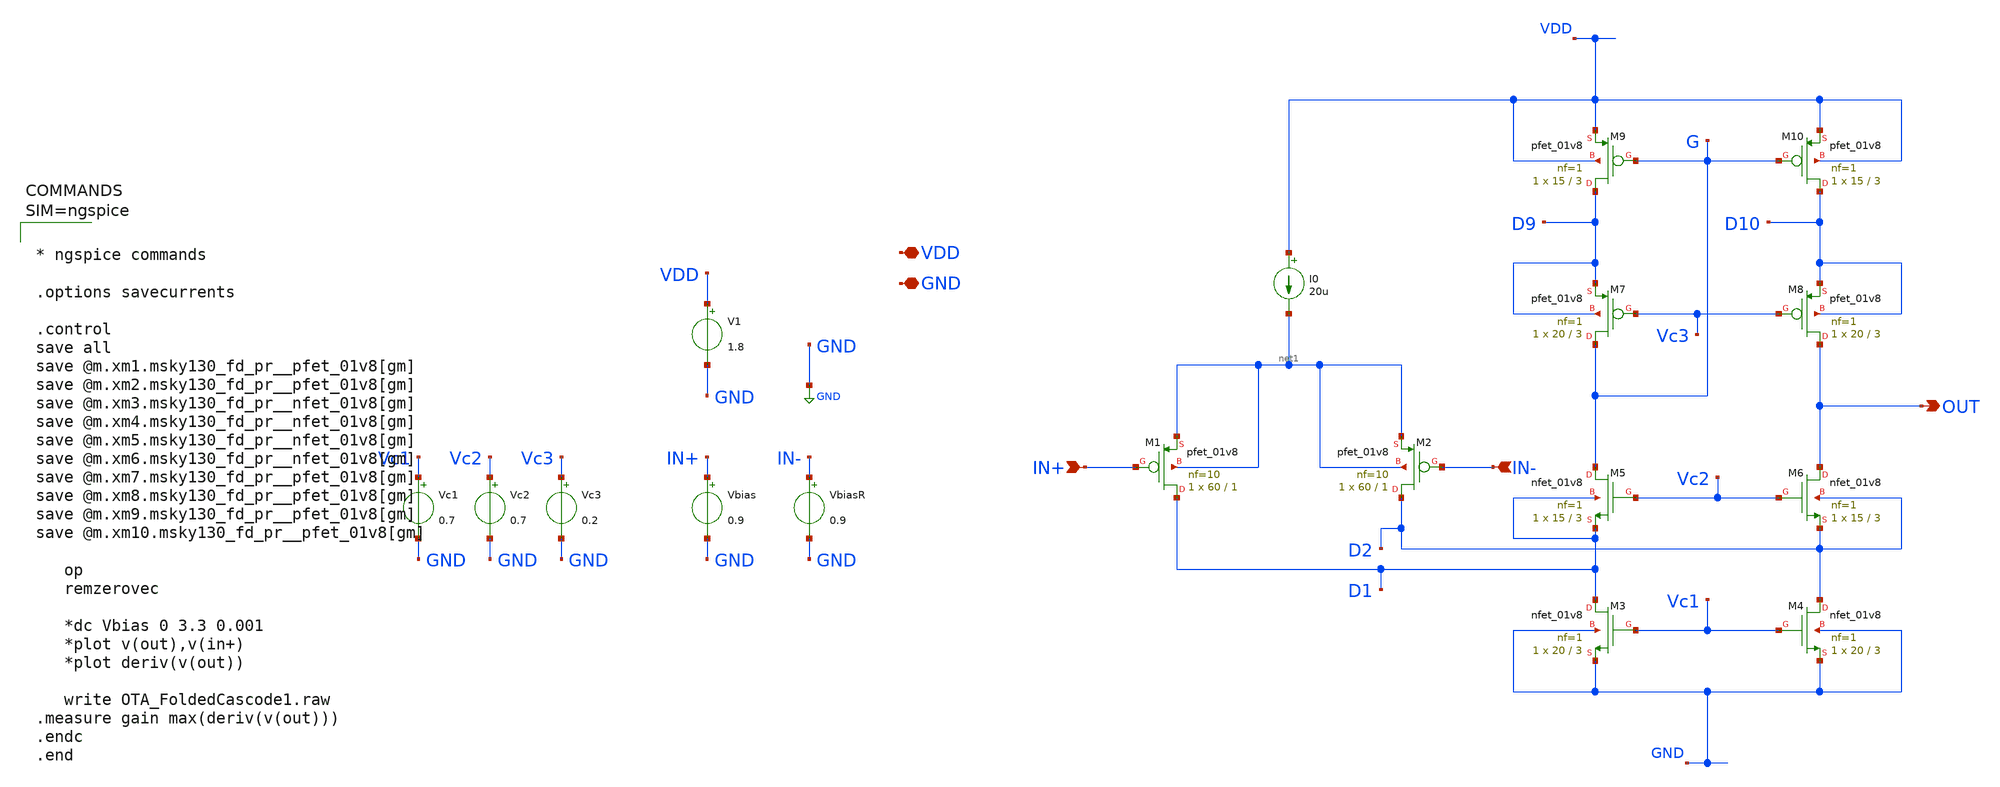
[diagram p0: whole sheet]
** sch_path: xschem/OTA_FoldedCascode1.sch
**.subckt OTA_FoldedCascode1 VDD GND IN+ IN- OUT
*.iopin VDD
*.iopin GND
*.ipin IN+
*.ipin IN-
*.opin OUT
V1 VDD GND 1.8
Vbias IN+ GND 0.9
VbiasR IN- GND 0.9
I0 VDD net1 20u
XM1 D1 IN+ net1 net1 sky130_fd_pr__pfet_01v8 L=1 W=60 nf=10 ad='int((nf+1)/2) * W/nf * 0.29' as='int((nf+2)/2) * W/nf * 0.29'
+ pd='2*int((nf+1)/2) * (W/nf + 0.29)' ps='2*int((nf+2)/2) * (W/nf + 0.29)' nrd='0.29 / W' nrs='0.29 / W'
+ sa=0 sb=0 sd=0 mult=1 m=1
XM2 D2 IN- net1 net1 sky130_fd_pr__pfet_01v8 L=1 W=60 nf=10 ad='int((nf+1)/2) * W/nf * 0.29' as='int((nf+2)/2) * W/nf * 0.29'
+ pd='2*int((nf+1)/2) * (W/nf + 0.29)' ps='2*int((nf+2)/2) * (W/nf + 0.29)' nrd='0.29 / W' nrs='0.29 / W'
+ sa=0 sb=0 sd=0 mult=1 m=1
XM3 D1 Vc1 GND GND sky130_fd_pr__nfet_01v8 L=3 W=20 nf=1 ad='int((nf+1)/2) * W/nf * 0.29' as='int((nf+2)/2) * W/nf * 0.29'
+ pd='2*int((nf+1)/2) * (W/nf + 0.29)' ps='2*int((nf+2)/2) * (W/nf + 0.29)' nrd='0.29 / W' nrs='0.29 / W'
+ sa=0 sb=0 sd=0 mult=1 m=1
XM4 D2 Vc1 GND GND sky130_fd_pr__nfet_01v8 L=3 W=20 nf=1 ad='int((nf+1)/2) * W/nf * 0.29' as='int((nf+2)/2) * W/nf * 0.29'
+ pd='2*int((nf+1)/2) * (W/nf + 0.29)' ps='2*int((nf+2)/2) * (W/nf + 0.29)' nrd='0.29 / W' nrs='0.29 / W'
+ sa=0 sb=0 sd=0 mult=1 m=1
XM5 G Vc2 D1 D1 sky130_fd_pr__nfet_01v8 L=3 W=15 nf=1 ad='int((nf+1)/2) * W/nf * 0.29' as='int((nf+2)/2) * W/nf * 0.29'
+ pd='2*int((nf+1)/2) * (W/nf + 0.29)' ps='2*int((nf+2)/2) * (W/nf + 0.29)' nrd='0.29 / W' nrs='0.29 / W'
+ sa=0 sb=0 sd=0 mult=1 m=1
XM6 OUT Vc2 D2 D2 sky130_fd_pr__nfet_01v8 L=3 W=15 nf=1 ad='int((nf+1)/2) * W/nf * 0.29' as='int((nf+2)/2) * W/nf * 0.29'
+ pd='2*int((nf+1)/2) * (W/nf + 0.29)' ps='2*int((nf+2)/2) * (W/nf + 0.29)' nrd='0.29 / W' nrs='0.29 / W'
+ sa=0 sb=0 sd=0 mult=1 m=1
XM7 G Vc3 D9 D9 sky130_fd_pr__pfet_01v8 L=3 W=20 nf=1 ad='int((nf+1)/2) * W/nf * 0.29' as='int((nf+2)/2) * W/nf * 0.29'
+ pd='2*int((nf+1)/2) * (W/nf + 0.29)' ps='2*int((nf+2)/2) * (W/nf + 0.29)' nrd='0.29 / W' nrs='0.29 / W'
+ sa=0 sb=0 sd=0 mult=1 m=1
XM8 OUT Vc3 D10 D10 sky130_fd_pr__pfet_01v8 L=3 W=20 nf=1 ad='int((nf+1)/2) * W/nf * 0.29' as='int((nf+2)/2) * W/nf * 0.29'
+ pd='2*int((nf+1)/2) * (W/nf + 0.29)' ps='2*int((nf+2)/2) * (W/nf + 0.29)' nrd='0.29 / W' nrs='0.29 / W'
+ sa=0 sb=0 sd=0 mult=1 m=1
XM9 D9 G VDD VDD sky130_fd_pr__pfet_01v8 L=3 W=15 nf=1 ad='int((nf+1)/2) * W/nf * 0.29' as='int((nf+2)/2) * W/nf * 0.29'
+ pd='2*int((nf+1)/2) * (W/nf + 0.29)' ps='2*int((nf+2)/2) * (W/nf + 0.29)' nrd='0.29 / W' nrs='0.29 / W'
+ sa=0 sb=0 sd=0 mult=1 m=1
XM10 D10 G VDD VDD sky130_fd_pr__pfet_01v8 L=3 W=15 nf=1 ad='int((nf+1)/2) * W/nf * 0.29' as='int((nf+2)/2) * W/nf * 0.29'
+ pd='2*int((nf+1)/2) * (W/nf + 0.29)' ps='2*int((nf+2)/2) * (W/nf + 0.29)' nrd='0.29 / W' nrs='0.29 / W'
+ sa=0 sb=0 sd=0 mult=1 m=1
Vc1 Vc1 GND 0.7
Vc2 Vc2 GND 0.7
Vc3 Vc3 GND 0.2
**** begin user architecture code



* ngspice commands

.options savecurrents

.control
save all
save @m.xm1.msky130_fd_pr__pfet_01v8[gm]
save @m.xm2.msky130_fd_pr__pfet_01v8[gm]
save @m.xm3.msky130_fd_pr__nfet_01v8[gm]
save @m.xm4.msky130_fd_pr__nfet_01v8[gm]
save @m.xm5.msky130_fd_pr__nfet_01v8[gm]
save @m.xm6.msky130_fd_pr__nfet_01v8[gm]
save @m.xm7.msky130_fd_pr__pfet_01v8[gm]
save @m.xm8.msky130_fd_pr__pfet_01v8[gm]
save @m.xm9.msky130_fd_pr__pfet_01v8[gm]
save @m.xm10.msky130_fd_pr__pfet_01v8[gm]

   op
   remzerovec

   *dc Vbias 0 3.3 0.001
   *plot v(out),v(in+)
   *plot deriv(v(out))

   write OTA_FoldedCascode1.raw
.measure gain max(deriv(v(out)))
.endc
.end



.lib $::SKYWATER_MODELS/sky130.lib.spice tt
**** end user architecture code
**.ends
.GLOBAL GND
.end
